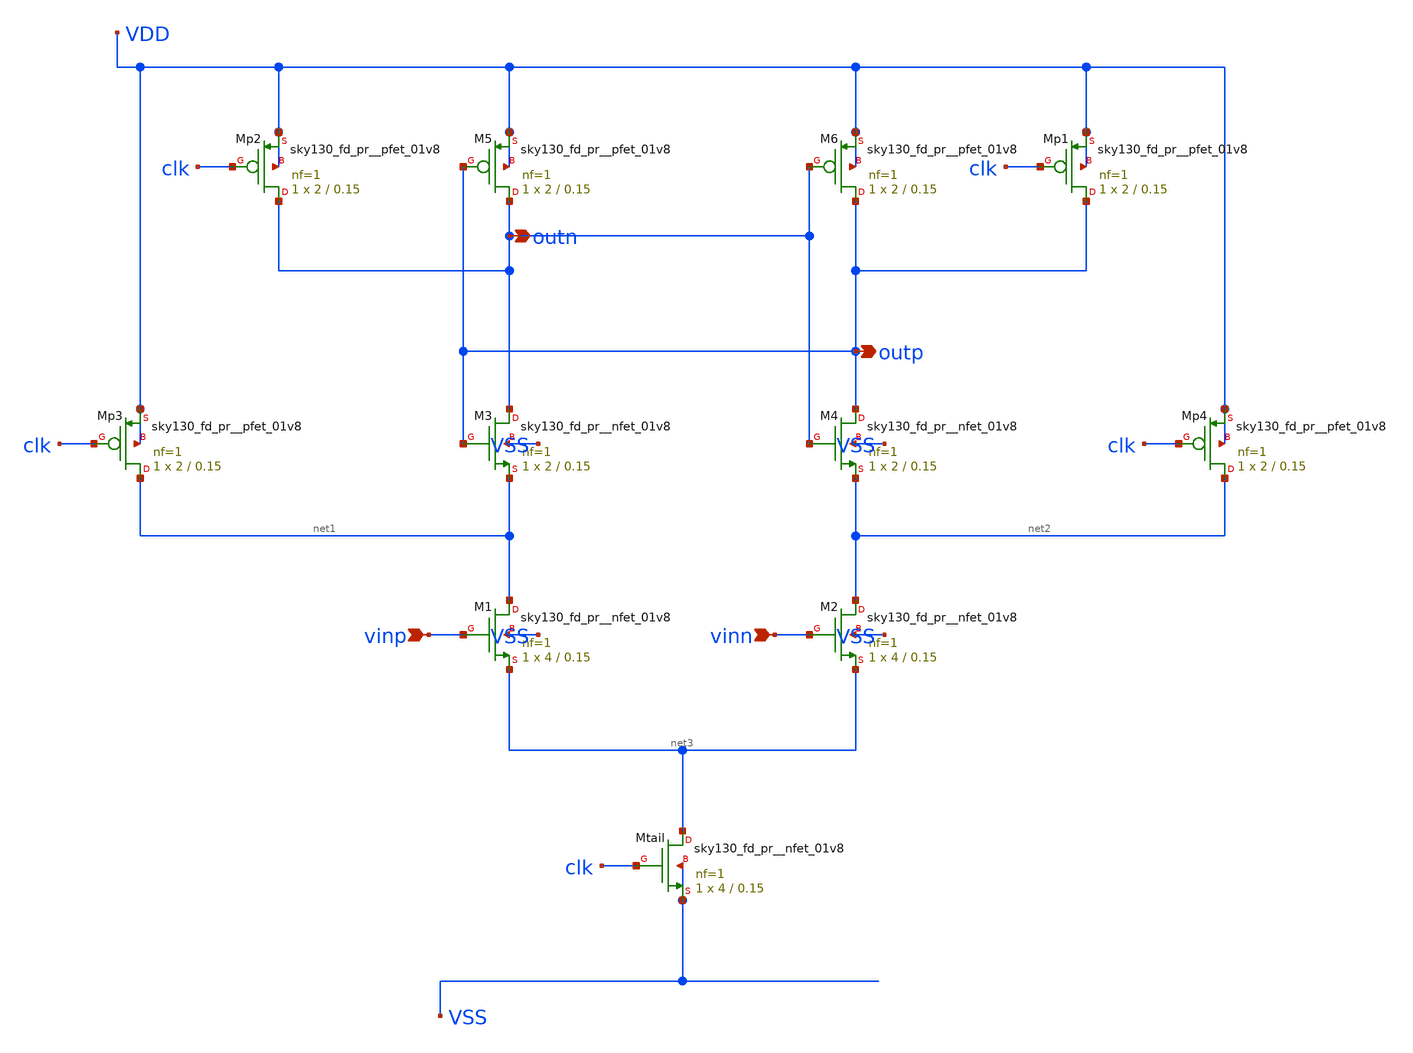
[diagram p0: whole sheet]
** sch_path: eda/hero/schematics/strongarm_sa.sch
**.subckt strongarm_sa vinp vinn outn outp
*.ipin vinp
*.ipin vinn
*.opin outn
*.opin outp
XM5 outn outp VDD VDD sky130_fd_pr__sky130_fd_pr__pfet_01v8 L=0.15 W=2 nf=1 ad='int((nf+1)/2) * W/nf * 0.29'
+ as='int((nf+2)/2) * W/nf * 0.29' pd='2*int((nf+1)/2) * (W/nf + 0.29)' ps='2*int((nf+2)/2) * (W/nf + 0.29)'
+ nrd='0.29 / W' nrs='0.29 / W' sa=0 sb=0 sd=0 mult=1 m=1
XM6 outp outn VDD VDD sky130_fd_pr__sky130_fd_pr__pfet_01v8 L=0.15 W=2 nf=1 ad='int((nf+1)/2) * W/nf * 0.29'
+ as='int((nf+2)/2) * W/nf * 0.29' pd='2*int((nf+1)/2) * (W/nf + 0.29)' ps='2*int((nf+2)/2) * (W/nf + 0.29)'
+ nrd='0.29 / W' nrs='0.29 / W' sa=0 sb=0 sd=0 mult=1 m=1
XMp2 outn clk VDD VDD sky130_fd_pr__sky130_fd_pr__pfet_01v8 L=0.15 W=2 nf=1 ad='int((nf+1)/2) * W/nf * 0.29'
+ as='int((nf+2)/2) * W/nf * 0.29' pd='2*int((nf+1)/2) * (W/nf + 0.29)' ps='2*int((nf+2)/2) * (W/nf + 0.29)'
+ nrd='0.29 / W' nrs='0.29 / W' sa=0 sb=0 sd=0 mult=1 m=1
XMp1 outp clk VDD VDD sky130_fd_pr__sky130_fd_pr__pfet_01v8 L=0.15 W=2 nf=1 ad='int((nf+1)/2) * W/nf * 0.29'
+ as='int((nf+2)/2) * W/nf * 0.29' pd='2*int((nf+1)/2) * (W/nf + 0.29)' ps='2*int((nf+2)/2) * (W/nf + 0.29)'
+ nrd='0.29 / W' nrs='0.29 / W' sa=0 sb=0 sd=0 mult=1 m=1
XM3 outn outp net1 VSS sky130_fd_pr__sky130_fd_pr__nfet_01v8 L=0.15 W=2 nf=1 ad='int((1 + 1)/2) * 2 / 1 * 0.29'
+ as='int((1 + 2)/2) * 2 / 1 * 0.29' pd='2*int((1 + 1)/2) * (2 / 1 + 0.29)' ps='2*int((1 + 2)/2) * (2 / 1 + 0.29)'
+ nrd='0.29 / 2 ' nrs='0.29 / 2 ' sa=0 sb=0 sd=0 mult=1 m=1
XM4 outp outn net2 VSS sky130_fd_pr__sky130_fd_pr__nfet_01v8 L=0.15 W=2 nf=1 ad='int((1 + 1)/2) * 2 / 1 * 0.29'
+ as='int((1 + 2)/2) * 2 / 1 * 0.29' pd='2*int((1 + 1)/2) * (2 / 1 + 0.29)' ps='2*int((1 + 2)/2) * (2 / 1 + 0.29)'
+ nrd='0.29 / 2 ' nrs='0.29 / 2 ' sa=0 sb=0 sd=0 mult=1 m=1
XMp3 net1 clk VDD VDD sky130_fd_pr__sky130_fd_pr__pfet_01v8 L=0.15 W=2 nf=1 ad='int((nf+1)/2) * W/nf * 0.29'
+ as='int((nf+2)/2) * W/nf * 0.29' pd='2*int((nf+1)/2) * (W/nf + 0.29)' ps='2*int((nf+2)/2) * (W/nf + 0.29)'
+ nrd='0.29 / W' nrs='0.29 / W' sa=0 sb=0 sd=0 mult=1 m=1
XMp4 net2 clk VDD VDD sky130_fd_pr__sky130_fd_pr__pfet_01v8 L=0.15 W=2 nf=1 ad='int((nf+1)/2) * W/nf * 0.29'
+ as='int((nf+2)/2) * W/nf * 0.29' pd='2*int((nf+1)/2) * (W/nf + 0.29)' ps='2*int((nf+2)/2) * (W/nf + 0.29)'
+ nrd='0.29 / W' nrs='0.29 / W' sa=0 sb=0 sd=0 mult=1 m=1
XM1 net1 vinp net3 VSS sky130_fd_pr__sky130_fd_pr__nfet_01v8 L=0.15 W=4 nf=1 ad='int((1 + 1)/2) * 4 / 1 * 0.29'
+ as='int((1 + 2)/2) * 4 / 1 * 0.29' pd='2*int((1 + 1)/2) * (4 / 1 + 0.29)' ps='2*int((1 + 2)/2) * (4 / 1 + 0.29)'
+ nrd='0.29 / 4 ' nrs='0.29 / 4 ' sa=0 sb=0 sd=0 mult=1 m=1
XM2 net2 vinn net3 VSS sky130_fd_pr__sky130_fd_pr__nfet_01v8 L=0.15 W=4 nf=1 ad='int((1 + 1)/2) * 4 / 1 * 0.29'
+ as='int((1 + 2)/2) * 4 / 1 * 0.29' pd='2*int((1 + 1)/2) * (4 / 1 + 0.29)' ps='2*int((1 + 2)/2) * (4 / 1 + 0.29)'
+ nrd='0.29 / 4 ' nrs='0.29 / 4 ' sa=0 sb=0 sd=0 mult=1 m=1
XMtail net3 clk VSS VSS sky130_fd_pr__sky130_fd_pr__nfet_01v8 L=0.15 W=4 nf=1 ad='int((1 + 1)/2) * 4 / 1 * 0.29'
+ as='int((1 + 2)/2) * 4 / 1 * 0.29' pd='2*int((1 + 1)/2) * (4 / 1 + 0.29)' ps='2*int((1 + 2)/2) * (4 / 1 + 0.29)'
+ nrd='0.29 / 4 ' nrs='0.29 / 4 ' sa=0 sb=0 sd=0 mult=1 m=1
**.ends
.end
